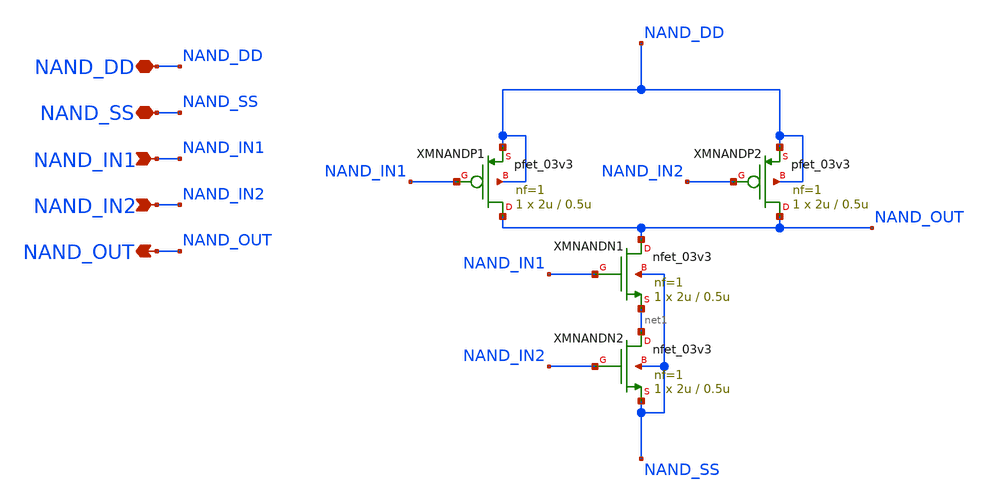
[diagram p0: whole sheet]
** sch_path: Design_Files/IC Design/Schematic/NAND2/NAND2.sch
**.subckt NAND2 NAND_DD NAND_SS NAND_IN1 NAND_OUT NAND_IN2
*.iopin NAND_DD
*.iopin NAND_SS
*.ipin NAND_IN1
*.opin NAND_OUT
*.ipin NAND_IN2
XMNANDP1 NAND_OUT NAND_IN1 NAND_DD NAND_DD pfet_03v3 L=0.5u W=2u nf=1 ad='int((nf+1)/2) * W/nf * 0.18u'
+ as='int((nf+2)/2) * W/nf * 0.18u' pd='2*int((nf+1)/2) * (W/nf + 0.18u)' ps='2*int((nf+2)/2) * (W/nf + 0.18u)'
+ nrd='0.18u / W' nrs='0.18u / W' sa=0 sb=0 sd=0 m=1
XMNANDN1 NAND_OUT NAND_IN1 net1 NAND_SS nfet_03v3 L=0.5u W=2u nf=1 ad='int((nf+1)/2) * W/nf * 0.18u'
+ as='int((nf+2)/2) * W/nf * 0.18u' pd='2*int((nf+1)/2) * (W/nf + 0.18u)' ps='2*int((nf+2)/2) * (W/nf + 0.18u)'
+ nrd='0.18u / W' nrs='0.18u / W' sa=0 sb=0 sd=0 m=1
XMNANDP2 NAND_OUT NAND_IN2 NAND_DD NAND_DD pfet_03v3 L=0.5u W=2u nf=1 ad='int((nf+1)/2) * W/nf * 0.18u'
+ as='int((nf+2)/2) * W/nf * 0.18u' pd='2*int((nf+1)/2) * (W/nf + 0.18u)' ps='2*int((nf+2)/2) * (W/nf + 0.18u)'
+ nrd='0.18u / W' nrs='0.18u / W' sa=0 sb=0 sd=0 m=1
XMNANDN2 net1 NAND_IN2 NAND_SS NAND_SS nfet_03v3 L=0.5u W=2u nf=1 ad='int((nf+1)/2) * W/nf * 0.18u' as='int((nf+2)/2) * W/nf * 0.18u'
+ pd='2*int((nf+1)/2) * (W/nf + 0.18u)' ps='2*int((nf+2)/2) * (W/nf + 0.18u)' nrd='0.18u / W' nrs='0.18u / W'
+ sa=0 sb=0 sd=0 m=1
**.ends
.end
